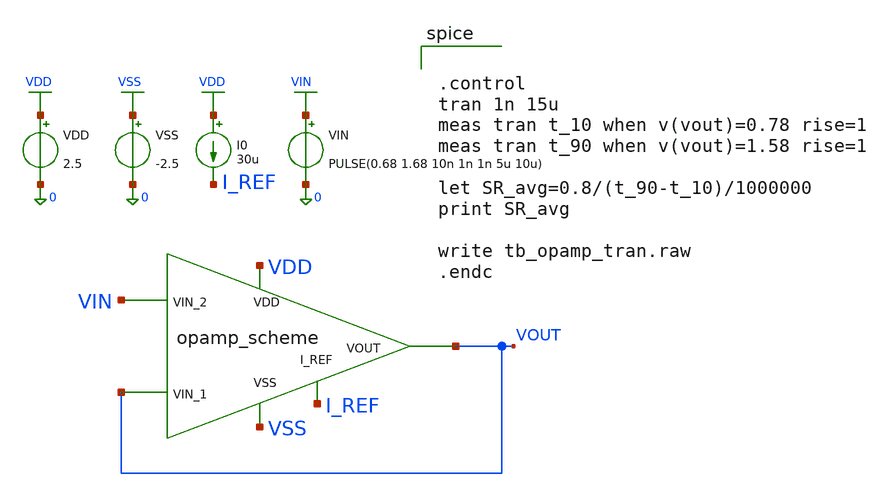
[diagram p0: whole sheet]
** sch_path: schematic/tb_opamp_tran.sch
**.subckt tb_opamp_tran
x1 VDD I_REF VOUT VIN VOUT VSS opamp_scheme
VDD VDD 0 2.5
VSS VSS 0 -2.5
I0 VDD I_REF 30u
VIN VIN 0 PULSE(0.68 1.68 10n 1n 1n 5u 10u)
**** begin user architecture code

.MODEL N_1u NMOS LEVEL  = 3
  TOX    = 200E-10         NSUB   = 1E17            GAMMA  = 0.5
  PHI    = 0.7             VTO    = 0.8             DELTA  = 3.0
  UO     = 650             ETA    = 3.0E-6          THETA  = 0.1
  KP     = 120E-6          VMAX   = 1E5             KAPPA  = 0.3
  RSH    = 0               NFS    = 1E12            TPG    = 1
  XJ     = 500E-9          LD     = 100E-9
  CGDO   = 200E-12         CGSO   = 200E-12         CGBO   = 1E-10
  CJ     = 400E-6          PB     = 1               MJ     = 0.5
  CJSW   = 300E-12         MJSW   = 0.5

*

.MODEL P_1u PMOS LEVEL  = 3
  TOX    = 200E-10         NSUB   = 1E17            GAMMA  = 0.6
  PHI    = 0.7             VTO    = -0.9            DELTA  = 0.1
  UO     = 250             ETA    = 0               THETA  = 0.1
  KP     = 40E-6           VMAX   = 5E4             KAPPA  = 1
  RSH    = 0               NFS    = 1E12            TPG    = -1
  XJ     = 500E-9          LD     = 100E-9
  CGDO   = 200E-12         CGSO   = 200E-12         CGBO   = 1E-10
  CJ     = 400E-6          PB     = 1               MJ     = 0.5
  CJSW   = 300E-12         MJSW   = 0.5



.param L=1u W1=3.5u W2=3.5u W3=10u W4=10u W5=3u W6=86.6u W7=13u W8=3u Cc=2.5p




.control
tran 1n 15u
meas tran t_10 when v(vout)=0.78 rise=1
meas tran t_90 when v(vout)=1.58 rise=1

let SR_avg=0.8/(t_90-t_10)/1000000
print SR_avg

write tb_opamp_tran.raw
.endc


**** end user architecture code
**.ends

* expanding   symbol:  opamp_scheme.sym # of pins=6
** sym_path: schematic/opamp_scheme.sym
** sch_path: schematic/opamp_scheme.sch
.subckt opamp_scheme VDD I_REF VOUT VIN_2 VIN_1 VSS
*.opin VOUT
*.ipin VIN_1
*.ipin VIN_2
*.ipin I_REF
*.ipin VDD
*.ipin VSS
V1 I_REF VBIAS 0
C1 net3 VOUT {Cc} m=1
M1 net1 VIN_1 net2 VSS N_1u w=W1 l=L m=1
M2 net3 VIN_2 net2 VSS N_1u w=W2 l=L m=1
M3 net1 net1 VDD VDD P_1u w=W3 l=L m=1
M4 net3 net1 VDD VDD P_1u w=W4 l=L m=1
M5 net2 VBIAS VSS VSS N_1u w=W5 l=L m=1
M6 VOUT net3 VDD VDD P_1u w=W6 l=L m=1
M7 VOUT VBIAS VSS VSS N_1u w=W7 l=L m=1
M8 VBIAS VBIAS VSS VSS N_1u w=W8 l=L m=1
.ends

.GLOBAL VDD
.GLOBAL VSS
.GLOBAL VIN
.end
